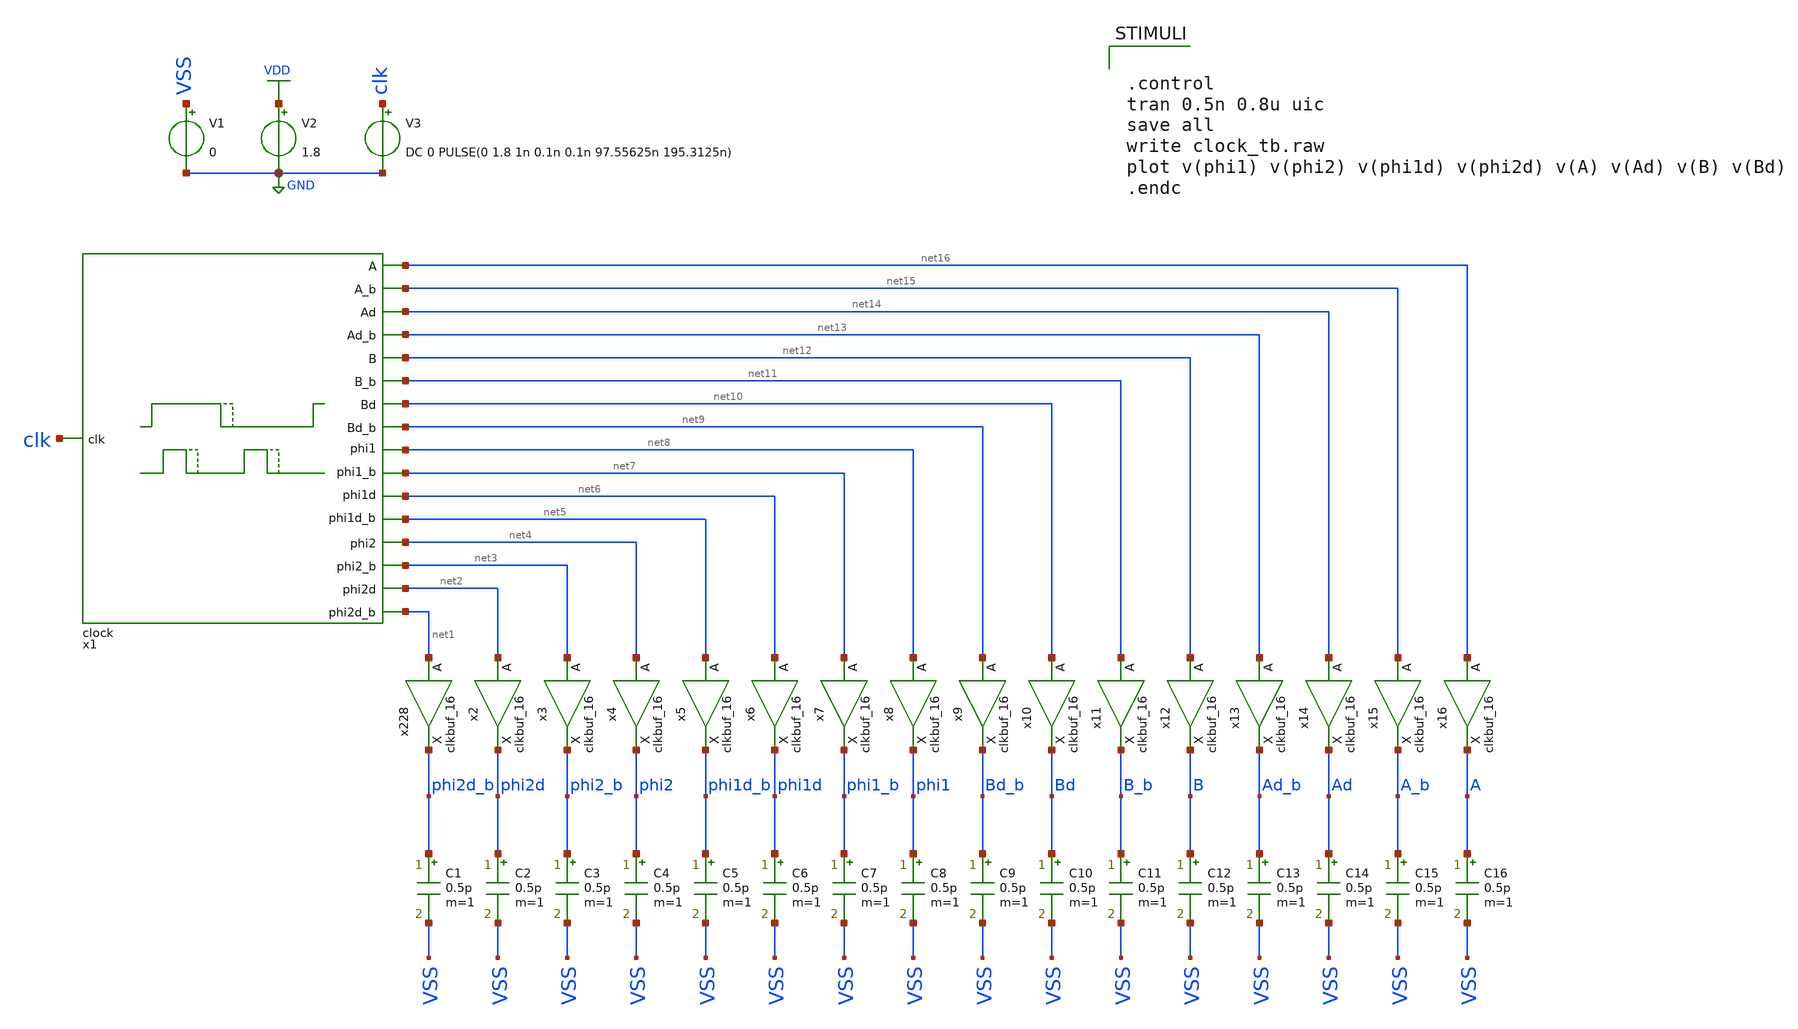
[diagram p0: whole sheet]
** sch_path: verification/analog_modulator/clock_tb.sch
**.subckt clock_tb
x1 net16 net15 net14 net13 net9 net10 net11 net12 net4 net3 net2 clk net1 net5 net6 net7 net8 VDD
+ VSS clock
V1 VSS GND 0
V2 VDD GND 1.8
V3 clk GND DC 0 PULSE(0 1.8 1n 0.1n 0.1n 97.55625n 195.3125n)
C1 phi2d_b VSS 0.5p m=1
C2 phi2d VSS 0.5p m=1
C3 phi2_b VSS 0.5p m=1
C4 phi2 VSS 0.5p m=1
C5 phi1d_b VSS 0.5p m=1
C6 phi1d VSS 0.5p m=1
C7 phi1_b VSS 0.5p m=1
C8 phi1 VSS 0.5p m=1
C9 Bd_b VSS 0.5p m=1
C10 Bd VSS 0.5p m=1
C11 B_b VSS 0.5p m=1
C12 B VSS 0.5p m=1
C13 Ad_b VSS 0.5p m=1
C14 Ad VSS 0.5p m=1
C15 A_b VSS 0.5p m=1
C16 A VSS 0.5p m=1
x228 net1 VSS VSS VDD VDD phi2d_b sky130_fd_sc_hd__clkbuf_16
x2 net2 VSS VSS VDD VDD phi2d sky130_fd_sc_hd__clkbuf_16
x3 net3 VSS VSS VDD VDD phi2_b sky130_fd_sc_hd__clkbuf_16
x4 net4 VSS VSS VDD VDD phi2 sky130_fd_sc_hd__clkbuf_16
x5 net5 VSS VSS VDD VDD phi1d_b sky130_fd_sc_hd__clkbuf_16
x6 net6 VSS VSS VDD VDD phi1d sky130_fd_sc_hd__clkbuf_16
x7 net7 VSS VSS VDD VDD phi1_b sky130_fd_sc_hd__clkbuf_16
x8 net8 VSS VSS VDD VDD phi1 sky130_fd_sc_hd__clkbuf_16
x9 net9 VSS VSS VDD VDD Bd_b sky130_fd_sc_hd__clkbuf_16
x10 net10 VSS VSS VDD VDD Bd sky130_fd_sc_hd__clkbuf_16
x11 net11 VSS VSS VDD VDD B_b sky130_fd_sc_hd__clkbuf_16
x12 net12 VSS VSS VDD VDD B sky130_fd_sc_hd__clkbuf_16
x13 net13 VSS VSS VDD VDD Ad_b sky130_fd_sc_hd__clkbuf_16
x14 net14 VSS VSS VDD VDD Ad sky130_fd_sc_hd__clkbuf_16
x15 net15 VSS VSS VDD VDD A_b sky130_fd_sc_hd__clkbuf_16
x16 net16 VSS VSS VDD VDD A sky130_fd_sc_hd__clkbuf_16
**** begin user architecture code

** opencircuitdesign pdks install
.lib /farmshare/home/classes/ee/372/PDKs/open_pdks_1.0.310/sky130/sky130A/libs.tech/ngspice/sky130.lib.spice tt
.inc /farmshare/home/classes/ee/372/PDKs/open_pdks_1.0.310/sky130/sky130A/libs.ref/sky130_fd_sc_hd/spice/sky130_fd_sc_hd.spice



.control
tran 0.5n 0.8u uic
save all
write clock_tb.raw
plot v(phi1) v(phi2) v(phi1d) v(phi2d) v(A) v(Ad) v(B) v(Bd)
.endc


**** end user architecture code
**.ends
.GLOBAL GND
.GLOBAL VDD
.end
